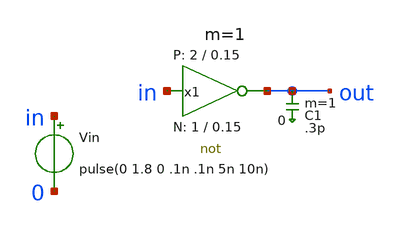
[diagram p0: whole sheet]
** sch_path: xschem/inv_tb.sch
* StefanSchippers/xschem_sky130/sky130_tests/not.sch:
* Copyright 2021 Stefan Frederik Schippers
* Licensed under the Apache License, Version 2.0 (the "License");
**.subckt inv_tb
x1 out in VCC VSS not W_N=1 L_N=0.15 W_P=2 L_P=0.15 m=1
Vin in 0 pulse(0 1.8 0 .1n .1n 5n 10n)
C1 out 0 .3p m=1
**** begin user architecture code
 .lib $::SKYWATER_MODELS/sky130.lib.spice tt


vvcc vcc 0 dc 1.8
vvss vss 0 dc 0
.param VCC=1.8
.tran 1n 25n
.save all alli
*.dc Vin 0 1.8 1m
*let abs_val = (abs(deriv(out)) >= 1) * 1.8
*.meas dc vth find v(in) when v(in)=v(out)
*.meas dc VOH find out=0.2
*.meas dc VOL find out=1.6
*.meas dc VIH find in when abs_out=1 cross=1
*.meas dc VIL find in when abs_out=1 cross=LAST


**** end user architecture code
**.ends

* expanding   symbol:  not.sym # of pins=2
** sym_path: not.sym
** sch_path: not.sch
.subckt not y a VCCPIN VSSPIN     W_N=1 L_N=0.15 W_P=2 L_P=0.15
*.opin y
*.ipin a
XM1 DN a VSSPIN VSSPIN sky130_fd_pr__nfet_01v8 L=L_N W=W_N nf=1 ad='int((1 + 1)/2) * W_N / 1 * 0.29'
+ as='int((1 + 2)/2) * W_N / 1 * 0.29' pd='2*int((1 + 1)/2) * (W_N / 1 + 0.29)' ps='2*int((1 + 2)/2) * (W_N / 1 + 0.29)'
+ nrd='0.29 / W_N ' nrs='0.29 / W_N ' sa=0 sb=0 sd=0 mult=1 m=1
XM2 DP a VCCPIN VCCPIN sky130_fd_pr__pfet_01v8 L=L_P W=W_P nf=1 ad='int((nf+1)/2) * W/nf * 0.29' as='int((nf+2)/2) * W/nf * 0.29'
+ pd='2*int((nf+1)/2) * (W/nf + 0.29)' ps='2*int((nf+2)/2) * (W/nf + 0.29)' nrd='0.29 / W' nrs='0.29 / W'
+ sa=0 sb=0 sd=0 mult=1 m=1
Vmeas DP y 0
.save i(vmeas)
Vmeas1 y DN 0
.save i(vmeas1)
.save v(dp)
.save v(dn)
.ends

.end
